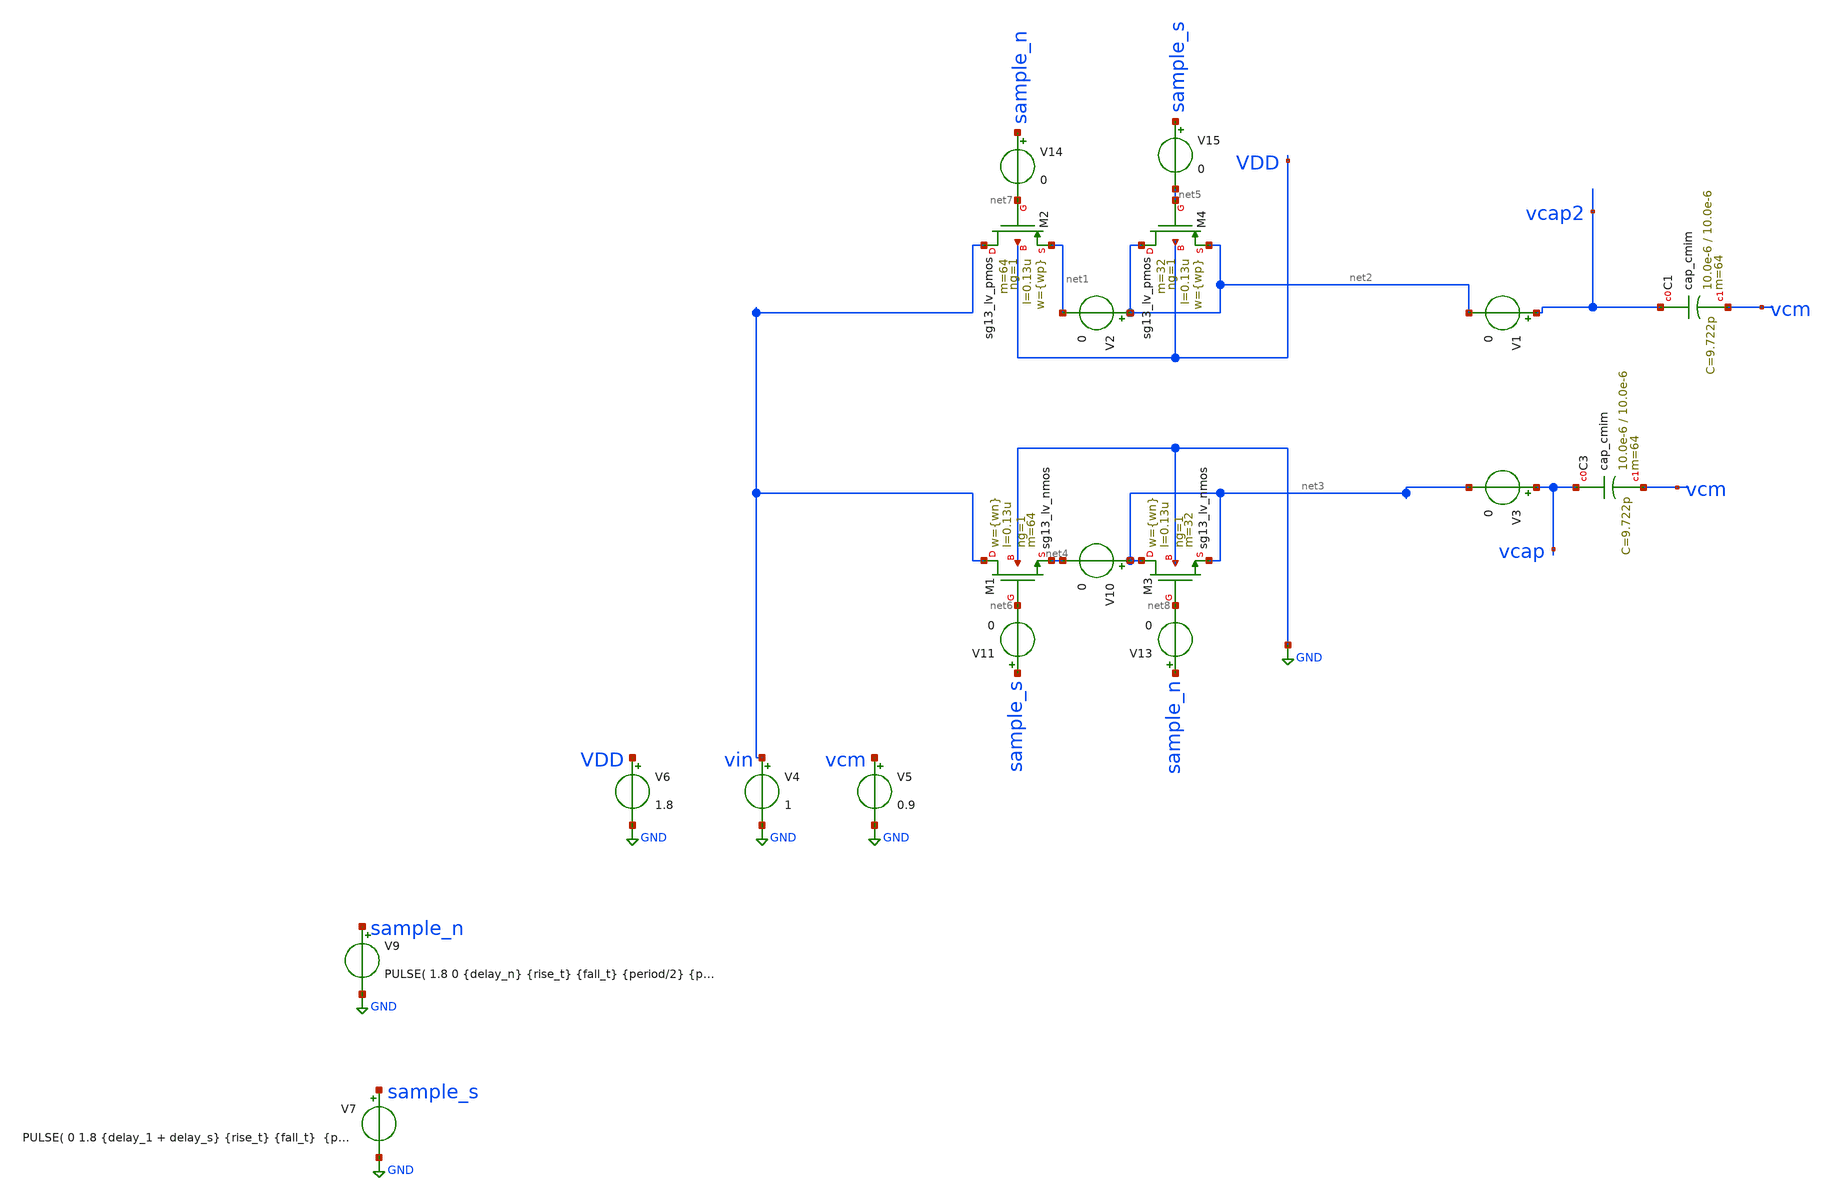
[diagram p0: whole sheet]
** sch_path: xschem/dac_icms_cell/testbenches/tb_dummy.sch
**.subckt tb_dummy
V1 vcap2 net2 0
V3 vcap net3 0
XM1 vin net6 net4 GND sg13_lv_nmos w={wn} l=0.13u ng=1 m=64 mm_ok=1
XM2 vin net7 net1 VDD sg13_lv_pmos w={wp} l=0.13u ng=1 m=64 mm_ok=1
XM3 net3 net8 net3 GND sg13_lv_nmos w={wn} l=0.13u ng=1 m=32 mm_ok=1
XM4 net2 net5 net2 VDD sg13_lv_pmos w={wp} l=0.13u ng=1 m=32 mm_ok=1
V4 vin GND 1
V5 vcm GND 0.9
V6 VDD GND 1.8
V7 sample_s GND PULSE( 0 1.8 {delay_1 + delay_s} {rise_t} {fall_t} {period/2} {period} 1)
V9 sample_n GND PULSE( 1.8 0 {delay_n} {rise_t} {fall_t} {period/2} {period} 1)
V2 net2 net1 0
V10 net3 net4 0
V11 sample_s net6 0
V13 sample_n net8 0
V14 sample_n net7 0
V15 sample_s net5 0
XC1 vcap2 vcm cap_cmim w=10.0e-6 l=10.0e-6 m=64 mm_ok=1
XC3 vcap vcm cap_cmim w=10.0e-6 l=10.0e-6 m=64 mm_ok=1
**** begin user architecture code



.lib cornerMOSlv.lib mos_tt
.lib cornerMOShv.lib mos_tt
.lib cornerHBT.lib hbt_typ
.lib cornerRES.lib res_typ
.lib cornerCAP.lib cap_typ





.param temp=27
.param period = 2n
.param wp = 5u
.param wn = 5u
.param rise_t = period*0.01
.param fall_t = period*0.01
.param delay_n = 0
.param delay_s = 0
.param delay_2 = 0
.param delay_1 = 0
.options savecurrents klu method=gear reltol=1e-2 abstol=1e-15 gmin=1e-10
.tran 1p {period}
.control

run
plot i(v1) i(v3)
plot sample_s sample_n sample_s2+2 sample_n2+2
plot i(v3)-i(v10) i(v10)
plot i(v1)-i(v2) i(v2)
plot i(v14) i(v15) i(v1)-i(v2) i(v2)

plot i(v11) i(v13) i(v3) i(v10)

plot vcap
.endc


**** end user architecture code
**.ends
.GLOBAL GND
.end
